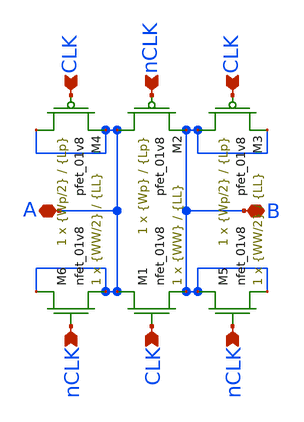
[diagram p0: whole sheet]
** sch_path: schematic/switch.sch
**.subckt switch B A CLK nCLK CLK CLK nCLK nCLK
*.iopin B
*.iopin A
*.ipin CLK
*.ipin nCLK
*.ipin CLK
*.ipin CLK
*.ipin nCLK
*.ipin nCLK
XM1 A CLK B GND sky130_fd_pr__nfet_01v8 L={LL} W={WW} nf=1 ad='int((nf+1)/2) * W/nf * 0.29' as='int((nf+2)/2) * W/nf * 0.29'
+ pd='2*int((nf+1)/2) * (W/nf + 0.29)' ps='2*int((nf+2)/2) * (W/nf + 0.29)' nrd='0.29 / W' nrs='0.29 / W'
+ sa=0 sb=0 sd=0 mult=1 m=1
XM2 A nCLK B VDD sky130_fd_pr__pfet_01v8 L={Lp} W={Wp} nf=1 ad='int((nf+1)/2) * W/nf * 0.29' as='int((nf+2)/2) * W/nf * 0.29'
+ pd='2*int((nf+1)/2) * (W/nf + 0.29)' ps='2*int((nf+2)/2) * (W/nf + 0.29)' nrd='0.29 / W' nrs='0.29 / W'
+ sa=0 sb=0 sd=0 mult=1 m=1
XM3 B CLK B VDD sky130_fd_pr__pfet_01v8 L={Lp} W={Wp/2} nf=1 ad='int((nf+1)/2) * W/nf * 0.29' as='int((nf+2)/2) * W/nf * 0.29'
+ pd='2*int((nf+1)/2) * (W/nf + 0.29)' ps='2*int((nf+2)/2) * (W/nf + 0.29)' nrd='0.29 / W' nrs='0.29 / W'
+ sa=0 sb=0 sd=0 mult=1 m=1
XM4 A CLK A VDD sky130_fd_pr__pfet_01v8 L={Lp} W={Wp/2} nf=1 ad='int((nf+1)/2) * W/nf * 0.29' as='int((nf+2)/2) * W/nf * 0.29'
+ pd='2*int((nf+1)/2) * (W/nf + 0.29)' ps='2*int((nf+2)/2) * (W/nf + 0.29)' nrd='0.29 / W' nrs='0.29 / W'
+ sa=0 sb=0 sd=0 mult=1 m=1
XM5 B nCLK B GND sky130_fd_pr__nfet_01v8 L={LL} W={WW/2} nf=1 ad='int((nf+1)/2) * W/nf * 0.29' as='int((nf+2)/2) * W/nf * 0.29'
+ pd='2*int((nf+1)/2) * (W/nf + 0.29)' ps='2*int((nf+2)/2) * (W/nf + 0.29)' nrd='0.29 / W' nrs='0.29 / W'
+ sa=0 sb=0 sd=0 mult=1 m=1
XM6 A nCLK A GND sky130_fd_pr__nfet_01v8 L={LL} W={WW/2} nf=1 ad='int((nf+1)/2) * W/nf * 0.29' as='int((nf+2)/2) * W/nf * 0.29'
+ pd='2*int((nf+1)/2) * (W/nf + 0.29)' ps='2*int((nf+2)/2) * (W/nf + 0.29)' nrd='0.29 / W' nrs='0.29 / W'
+ sa=0 sb=0 sd=0 mult=1 m=1
**.ends
.end
